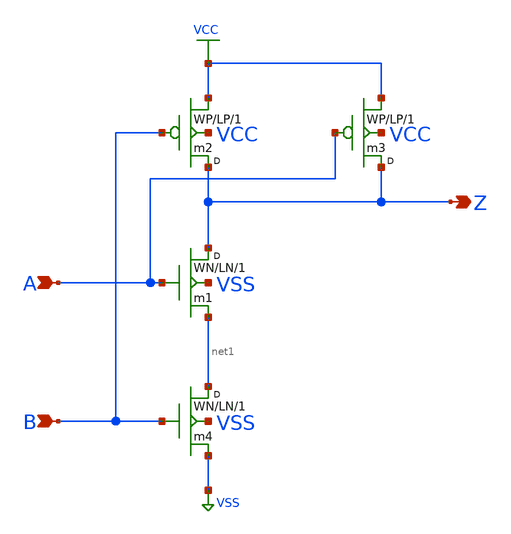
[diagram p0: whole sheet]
** sch_path: xschem_library/examples/nand2.sch
**.subckt nand2 A Z B
*.ipin A
*.opin Z
*.ipin B
m1 Z A net1 VSS nmos w=WN l=LN m=1
m2 Z B VCC VCC pmos w=WP l=LP m=1
m3 Z A VCC VCC pmos w=WP l=LP m=1
m4 net1 B VSS VSS nmos w=WN l=LN m=1
**.ends
.GLOBAL VCC
.GLOBAL VSS
.end
